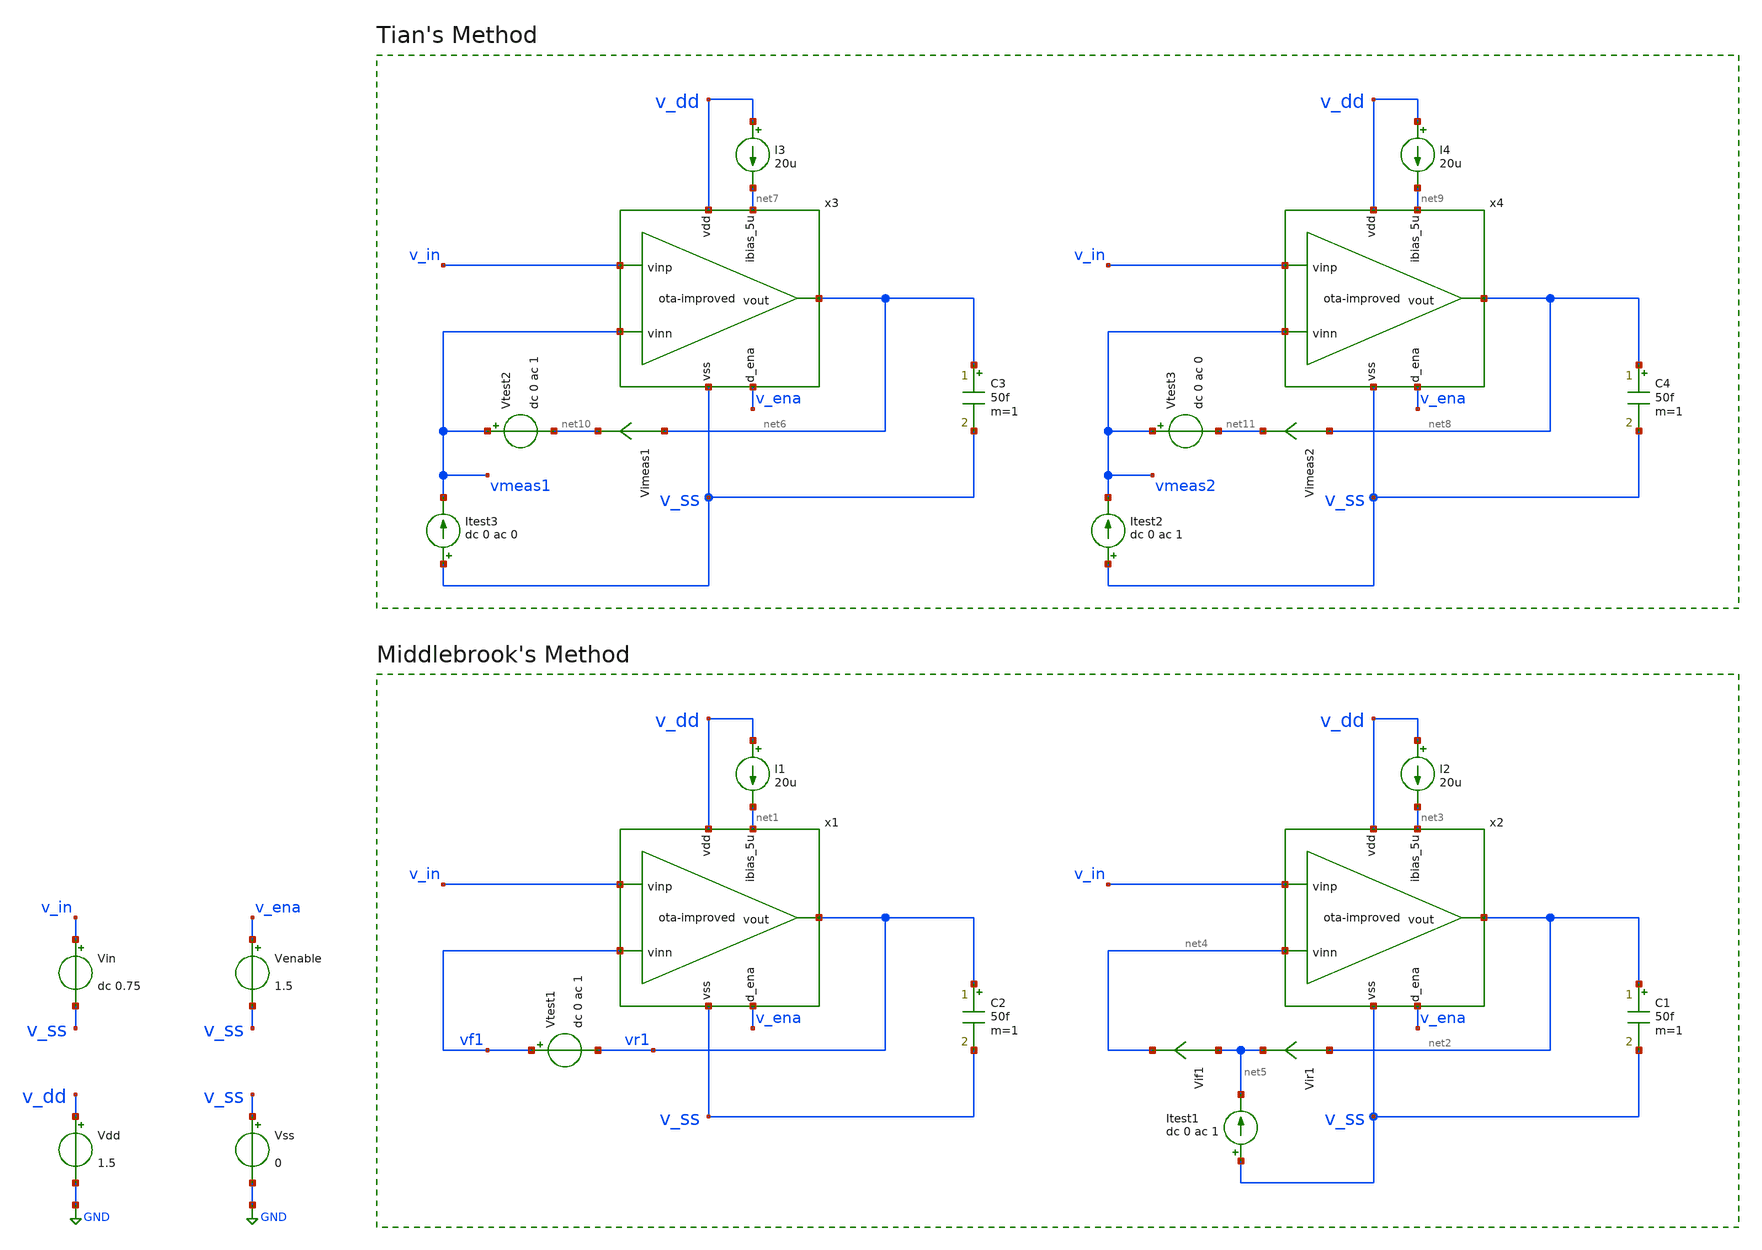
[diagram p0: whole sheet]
** sch_path: xschem/ota-improved_tb-loopgain.sch
* (c) 2024 H. Pretl, S. Dorrer, Apache-2.0 license
**.subckt ota-improved_tb-loopgain
Vdd v_dd GND 1.5
Vss v_ss GND 0
Vin v_in v_ss dc 0.75
Venable v_ena v_ss 1.5
C2 vr1 v_ss 50f m=1
I1 v_dd net1 20u
Vtest1 vf1 vr1 dc 0 ac 1
C1 net2 v_ss 50f m=1
I2 v_dd net3 20u
Vir1 net2 net5 0
.save i(vir1)
Vif1 net5 net4 0
.save i(vif1)
Itest1 v_ss net5 dc 0 ac 1
C3 net6 v_ss 50f m=1
I3 v_dd net7 20u
C4 net8 v_ss 50f m=1
I4 v_dd net9 20u
Itest3 v_ss vmeas1 dc 0 ac 0
Vtest2 vmeas1 net10 dc 0 ac 1
Vimeas1 net6 net10 0
.save i(vimeas1)
Itest2 v_ss vmeas2 dc 0 ac 1
Vtest3 vmeas2 net11 dc 0 ac 0
Vimeas2 net8 net11 0
.save i(vimeas2)
x1 v_dd vr1 v_in vf1 net1 v_ena v_ss ota-improved
x2 v_dd net2 v_in net4 net3 v_ena v_ss ota-improved
x3 v_dd net6 v_in vmeas1 net7 v_ena v_ss ota-improved
x4 v_dd net8 v_in vmeas2 net9 v_ena v_ss ota-improved
**** begin user architecture code
 .lib cornerMOSlv.lib mos_tt



.param temp=27
.options savecurrents reltol=1e-3 abstol=1e-12 gmin=1e-15
.control
save all

* Operating Point Analysis
op
remzerovec
write ota-improved_tb-loopgain.raw
set appendwrite

* AC Analysis
ac dec 101 1 100G
remzerovec
write ota-improved_tb-loopgain.raw
set appendwrite

* Middlebrook's Method
let tv=-v(vr1)/v(vf1)
let ti=-i(vir1)/i(vif1)
let tmb=(tv*ti - 1)/(tv + ti + 2)

plot db(tmb) ylabel 'Magnitude - Middlebrook'
plot 180/pi*cphase(tmb) ylabel 'Phase - Middlebrook'

* Tian's Method
* vtest=0, itest=1:
let A=i(Vimeas2)
let C=v(vmeas2)

* vtest=1, itest=0:
let B=i(Vimeas1)
let D=v(vmeas1)
let ttian=(A*D-B*C-A)/(2*(B*C-A*D)+A-D+1)

plot db(ttian) ylabel 'Magnitude - Tian'
plot 180/pi*cphase(ttian) ylabel 'Phase - Tian'

* Middlebrook vs. Tian
plot db(tmb) db(ttian) ylabel 'Magnitude'
plot 180/pi*cphase(tmb) 180/pi*cphase(ttian) ylabel 'Phase'

write ota-improved_tb-loopgain.raw

*quit
.endc


 .lib cornerRES.lib res_typ

**** end user architecture code
**.ends
.GLOBAL GND
.end
